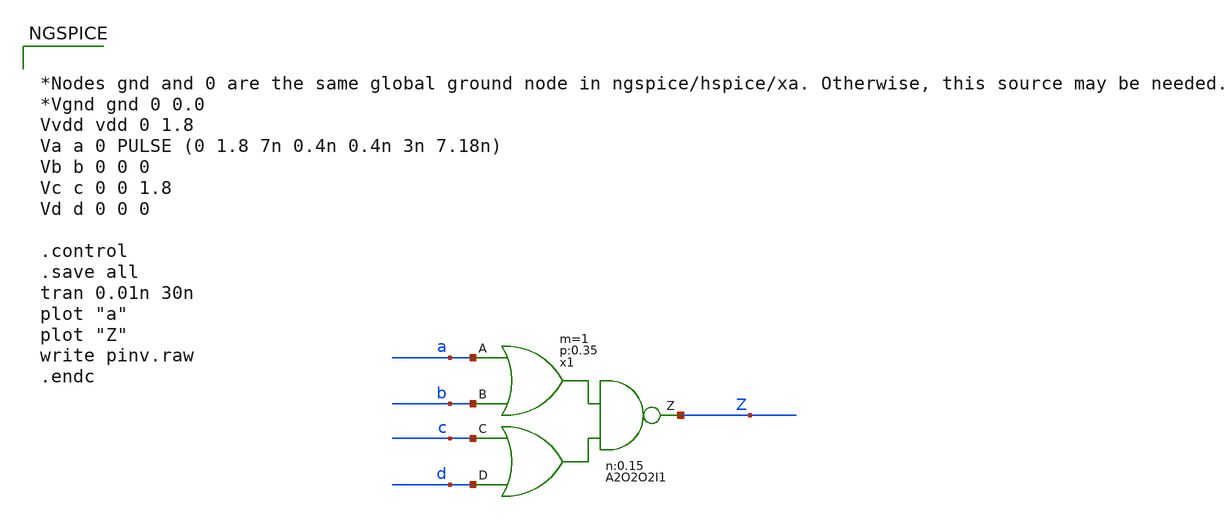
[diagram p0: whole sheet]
** sch_path: skywater-tests/test_A20202I1.sch
**.subckt test_A20202I1
x1 a b c d Z vdd gnd A2O2O2I1 W_N=60 L_N=0.15 W_P=60 L_P=0.35 m=1
**** begin user architecture code

.include $::SKYWATER_MODELS/cells/nfet_01v8/sky130_fd_pr__nfet_01v8__tt.corner.spice
.include $::SKYWATER_MODELS/cells/pfet_01v8/sky130_fd_pr__pfet_01v8__tt.corner.spice
* Mismatch parameters
.include $::SKYWATER_MODELS/cells/nfet_01v8/sky130_fd_pr__nfet_01v8__mismatch.corner.spice
.include $::SKYWATER_MODELS/cells/pfet_01v8/sky130_fd_pr__pfet_01v8__mismatch.corner.spice

* All models
.include $::SKYWATER_MODELS/models/all.spice



*Nodes gnd and 0 are the same global ground node in ngspice/hspice/xa. Otherwise, this source may be
*+ needed.
*Vgnd gnd 0 0.0
Vvdd vdd 0 1.8
Va a 0 PULSE (0 1.8 7n 0.4n 0.4n 3n 7.18n)
Vb b 0 0 0
Vc c 0 0 1.8
Vd d 0 0 0

.control
.save all
tran 0.01n 30n
plot "a"
plot "Z"
write pinv.raw
.endc


**** end user architecture code
**.ends

* expanding   symbol:  A2O2O2I1.sym # of pins=5
** sym_path: skywater-tests/A2O2O2I1.sym
** sch_path: skywater-tests/A2O2O2I1.sch
.subckt A2O2O2I1 A B C D Z VCCPIN VSSPIN     W_N=1 L_N=0.15 W_P=2 L_P=0.35
*.ipin B
*.opin Z
*.ipin A
*.ipin D
*.ipin C
XMnA Z A net1 VSSPIN sky130_fd_pr__nfet_01v8 L=L_N W=W_N nf=1 ad='int((nf+1)/2) * W/nf * 0.29' as='int((nf+2)/2) * W/nf * 0.29'
+ pd='2*int((nf+1)/2) * (W/nf + 0.29)' ps='2*int((nf+2)/2) * (W/nf + 0.29)' nrd='0.29 / W' nrs='0.29 / W'
+ sa=0 sb=0 sd=0 mult=1 m=1
XMpB net2 B VCCPIN VCCPIN sky130_fd_pr__pfet_01v8 L=L_P W=W_P nf=1 ad='int((nf+1)/2) * W/nf * 0.29' as='int((nf+2)/2) * W/nf * 0.29'
+ pd='2*int((nf+1)/2) * (W/nf + 0.29)' ps='2*int((nf+2)/2) * (W/nf + 0.29)' nrd='0.29 / W' nrs='0.29 / W'
+ sa=0 sb=0 sd=0 mult=1 m=1
XMnB Z B net1 VSSPIN sky130_fd_pr__nfet_01v8 L=L_N W=W_N nf=1 ad='int((nf+1)/2) * W/nf * 0.29' as='int((nf+2)/2) * W/nf * 0.29'
+ pd='2*int((nf+1)/2) * (W/nf + 0.29)' ps='2*int((nf+2)/2) * (W/nf + 0.29)' nrd='0.29 / W' nrs='0.29 / W'
+ sa=0 sb=0 sd=0 mult=1 m=1
XMnC net1 C VSSPIN VSSPIN sky130_fd_pr__nfet_01v8 L=L_N W=W_N nf=1 ad='int((nf+1)/2) * W/nf * 0.29' as='int((nf+2)/2) * W/nf * 0.29'
+ pd='2*int((nf+1)/2) * (W/nf + 0.29)' ps='2*int((nf+2)/2) * (W/nf + 0.29)' nrd='0.29 / W' nrs='0.29 / W'
+ sa=0 sb=0 sd=0 mult=1 m=1
XMnD net1 D VSSPIN VSSPIN sky130_fd_pr__nfet_01v8 L=L_N W=W_N nf=1 ad='int((nf+1)/2) * W/nf * 0.29' as='int((nf+2)/2) * W/nf * 0.29'
+ pd='2*int((nf+1)/2) * (W/nf + 0.29)' ps='2*int((nf+2)/2) * (W/nf + 0.29)' nrd='0.29 / W' nrs='0.29 / W'
+ sa=0 sb=0 sd=0 mult=1 m=1
XMpA Z A net2 VCCPIN sky130_fd_pr__pfet_01v8 L=L_P W=W_P nf=1 ad='int((nf+1)/2) * W/nf * 0.29' as='int((nf+2)/2) * W/nf * 0.29'
+ pd='2*int((nf+1)/2) * (W/nf + 0.29)' ps='2*int((nf+2)/2) * (W/nf + 0.29)' nrd='0.29 / W' nrs='0.29 / W'
+ sa=0 sb=0 sd=0 mult=1 m=1
XMpD net3 D VCCPIN VCCPIN sky130_fd_pr__pfet_01v8 L=L_P W=W_P nf=1 ad='int((nf+1)/2) * W/nf * 0.29' as='int((nf+2)/2) * W/nf * 0.29'
+ pd='2*int((nf+1)/2) * (W/nf + 0.29)' ps='2*int((nf+2)/2) * (W/nf + 0.29)' nrd='0.29 / W' nrs='0.29 / W'
+ sa=0 sb=0 sd=0 mult=1 m=1
XMpC Z C net3 VCCPIN sky130_fd_pr__pfet_01v8 L=L_P W=W_P nf=1 ad='int((nf+1)/2) * W/nf * 0.29' as='int((nf+2)/2) * W/nf * 0.29'
+ pd='2*int((nf+1)/2) * (W/nf + 0.29)' ps='2*int((nf+2)/2) * (W/nf + 0.29)' nrd='0.29 / W' nrs='0.29 / W'
+ sa=0 sb=0 sd=0 mult=1 m=1
.ends

.end
